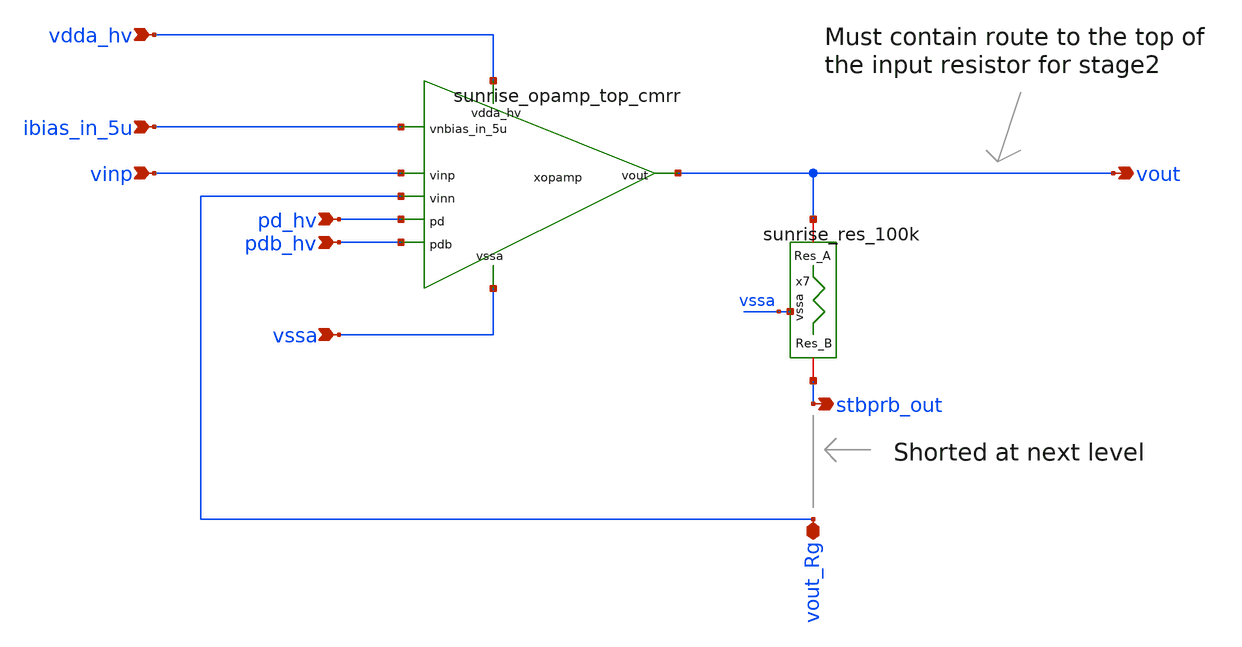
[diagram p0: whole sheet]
** sch_path: Schematics_Layout/sunrise_NIA_loop/sunrise_NIA_loop.sch
**.subckt sunrise_NIA_loop pd_hv pdb_hv ibias_in_5u vinp vdda_hv vssa vout stbprb_out vout_Rg
*.ipin pd_hv
*.ipin pdb_hv
*.ipin ibias_in_5u
*.ipin vinp
*.ipin vdda_hv
*.ipin vssa
*.opin vout
*.opin stbprb_out
*.iopin vout_Rg
x7 vssa stbprb_out vout sunrise_res_100k
xopamp vdda_hv ibias_in_5u vout vinp vout_Rg pd_hv pdb_hv vssa sunrise_opamp_top_cmrr
**.ends
.end
